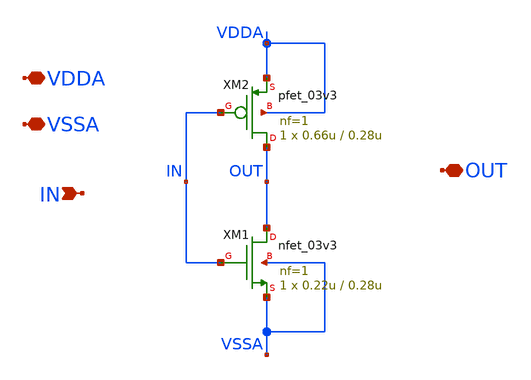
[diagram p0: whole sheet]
** sch_path: SAR_ADC/blocks/tracking_switches/tracking_switches_inv_1x.sch
**.subckt tracking_switches_inv_1x VDDA VSSA OUT IN
*.iopin VDDA
*.iopin VSSA
*.iopin OUT
*.ipin IN
XM1 OUT IN VSSA VSSA nfet_03v3 L=0.28u W=0.22u nf=1 ad='int((nf+1)/2) * W/nf * 0.18u' as='int((nf+2)/2) * W/nf * 0.18u'
+ pd='2*int((nf+1)/2) * (W/nf + 0.18u)' ps='2*int((nf+2)/2) * (W/nf + 0.18u)' nrd='0.18u / W' nrs='0.18u / W'
+ sa=0 sb=0 sd=0 m=1
XM2 OUT IN VDDA VDDA pfet_03v3 L=0.28u W=0.66u nf=1 ad='int((nf+1)/2) * W/nf * 0.18u' as='int((nf+2)/2) * W/nf * 0.18u'
+ pd='2*int((nf+1)/2) * (W/nf + 0.18u)' ps='2*int((nf+2)/2) * (W/nf + 0.18u)' nrd='0.18u / W' nrs='0.18u / W'
+ sa=0 sb=0 sd=0 m=1
**.ends
.end
